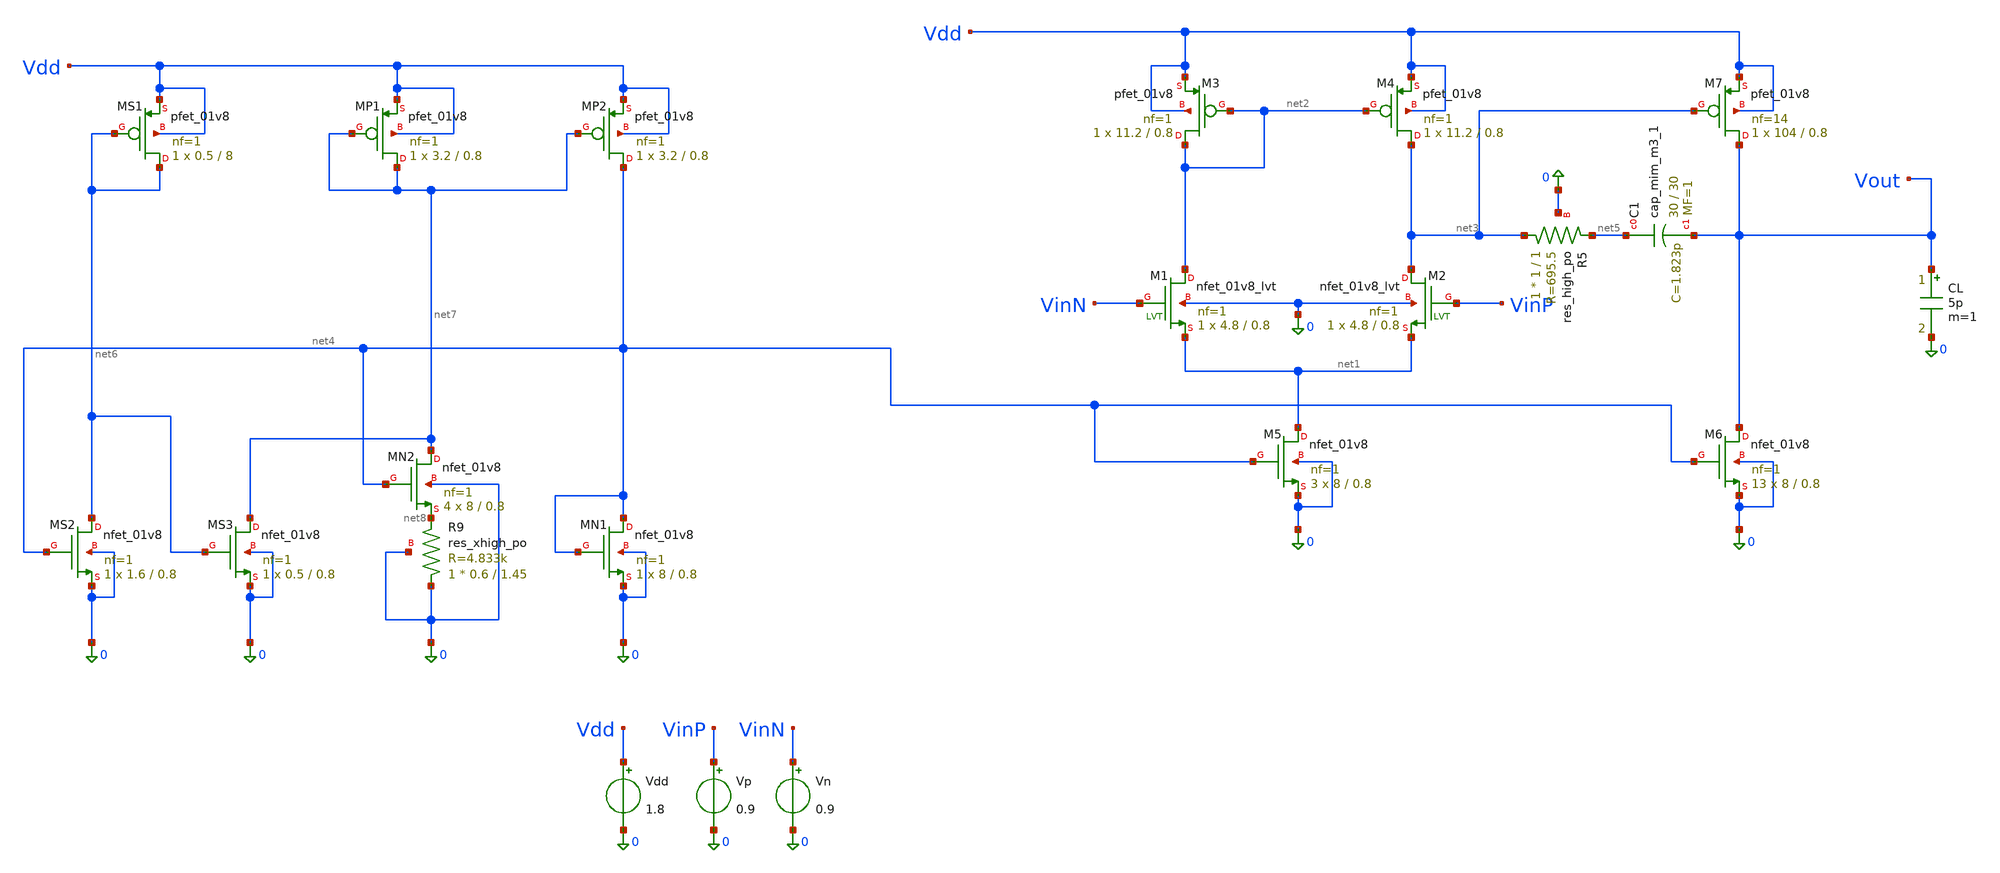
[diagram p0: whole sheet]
** sch_path: parameter_extraction/opamp.sch
**.subckt opamp
XM1 net2 VinN net1 0 sky130_fd_pr__nfet_01v8_lvt L=0.8 W=4.8 nf=1 ad='int((1 + 1)/2) * 4.8 / 1 * 0.29'
+ as='int((1 + 2)/2) * 4.8 / 1 * 0.29' pd='2*int((1 + 1)/2) * (4.8 / 1 + 0.29)' ps='2*int((1 + 2)/2) * (4.8 / 1 + 0.29)'
+ nrd='0.29 / 4.8 ' nrs='0.29 / 4.8 ' sa=0 sb=0 sd=0 mult=1 m=1
XM3 net2 net2 Vdd Vdd sky130_fd_pr__pfet_01v8 L=0.8 W=11.2 nf=1 ad='int((1 + 1)/2) * 11.2 / 1 * 0.29'
+ as='int((1 + 2)/2) * 11.2 / 1 * 0.29' pd='2*int((1 + 1)/2) * (11.2 / 1 + 0.29)' ps='2*int((1 + 2)/2) * (11.2 / 1 + 0.29)'
+ nrd='0.29 / 11.2 ' nrs='0.29 / 11.2 ' sa=0 sb=0 sd=0 mult=1 m=1
XM5 net1 net4 0 0 sky130_fd_pr__nfet_01v8 L=0.8 W=8 nf=1 ad='int((1 + 1)/2) * 8 / 1 * 0.29' as='int((1 + 2)/2) * 8 / 1 * 0.29'
+ pd='2*int((1 + 1)/2) * (8 / 1 + 0.29)' ps='2*int((1 + 2)/2) * (8 / 1 + 0.29)' nrd='0.29 / 8 ' nrs='0.29 / 8 '
+ sa=0 sb=0 sd=0 mult=3 m=3
XM2 net3 VinP net1 0 sky130_fd_pr__nfet_01v8_lvt L=0.8 W=4.8 nf=1 ad='int((1 + 1)/2) * 4.8 / 1 * 0.29'
+ as='int((1 + 2)/2) * 4.8 / 1 * 0.29' pd='2*int((1 + 1)/2) * (4.8 / 1 + 0.29)' ps='2*int((1 + 2)/2) * (4.8 / 1 + 0.29)'
+ nrd='0.29 / 4.8 ' nrs='0.29 / 4.8 ' sa=0 sb=0 sd=0 mult=1 m=1
XM4 net3 net2 Vdd Vdd sky130_fd_pr__pfet_01v8 L=0.8 W=11.2 nf=1 ad='int((1 + 1)/2) * 11.2 / 1 * 0.29'
+ as='int((1 + 2)/2) * 11.2 / 1 * 0.29' pd='2*int((1 + 1)/2) * (11.2 / 1 + 0.29)' ps='2*int((1 + 2)/2) * (11.2 / 1 + 0.29)'
+ nrd='0.29 / 11.2 ' nrs='0.29 / 11.2 ' sa=0 sb=0 sd=0 mult=1 m=1
XM6 Vout net4 0 0 sky130_fd_pr__nfet_01v8 L=0.8 W=8 nf=1 ad='int((1 + 1)/2) * 8 / 1 * 0.29' as='int((1 + 2)/2) * 8 / 1 * 0.29'
+ pd='2*int((1 + 1)/2) * (8 / 1 + 0.29)' ps='2*int((1 + 2)/2) * (8 / 1 + 0.29)' nrd='0.29 / 8 ' nrs='0.29 / 8 '
+ sa=0 sb=0 sd=0 mult=13 m=13
XM7 Vout net3 Vdd Vdd sky130_fd_pr__pfet_01v8 L=0.8 W=104 nf=14 ad='int((14 + 1)/2) * 104 / 14 * 0.29'
+ as='int((14 + 2)/2) * 104 / 14 * 0.29' pd='2*int((14 + 1)/2) * (104 / 14 + 0.29)' ps='2*int((14 + 2)/2) * (104 / 14 + 0.29)'
+ nrd='0.29 / 104 ' nrs='0.29 / 104 ' sa=0 sb=0 sd=0 mult=1 m=1
XC1 net5 Vout sky130_fd_pr__cap_mim_m3_1 W=30 L=30 MF=1 m=1
Vdd Vdd 0 1.8
Vp VinP 0 0.9
Vn VinN 0 0.9
XR5 net3 net5 0 sky130_fd_pr__res_high_po W=1 L=1 mult=1 m=1
CL Vout 0 5p m=1
XMS1 net6 net6 Vdd Vdd sky130_fd_pr__pfet_01v8 L=8 W=0.5 nf=1 ad='int((1 + 1)/2) * 0.5 / 1 * 0.29' as='int((1 + 2)/2) * 0.5 / 1 * 0.29'
+ pd='2*int((1 + 1)/2) * (0.5 / 1 + 0.29)' ps='2*int((1 + 2)/2) * (0.5 / 1 + 0.29)' nrd='0.29 / 0.5 ' nrs='0.29 / 0.5 '
+ sa=0 sb=0 sd=0 mult=1 m=1
XMP1 net7 net7 Vdd Vdd sky130_fd_pr__pfet_01v8 L=0.8 W=3.2 nf=1 ad='int((1 + 1)/2) * 3.2 / 1 * 0.29'
+ as='int((1 + 2)/2) * 3.2 / 1 * 0.29' pd='2*int((1 + 1)/2) * (3.2 / 1 + 0.29)' ps='2*int((1 + 2)/2) * (3.2 / 1 + 0.29)'
+ nrd='0.29 / 3.2 ' nrs='0.29 / 3.2 ' sa=0 sb=0 sd=0 mult=1 m=1
XMP2 net4 net7 Vdd Vdd sky130_fd_pr__pfet_01v8 L=0.8 W=3.2 nf=1 ad='int((1 + 1)/2) * 3.2 / 1 * 0.29'
+ as='int((1 + 2)/2) * 3.2 / 1 * 0.29' pd='2*int((1 + 1)/2) * (3.2 / 1 + 0.29)' ps='2*int((1 + 2)/2) * (3.2 / 1 + 0.29)'
+ nrd='0.29 / 3.2 ' nrs='0.29 / 3.2 ' sa=0 sb=0 sd=0 mult=1 m=1
XR9 0 net8 0 sky130_fd_pr__res_xhigh_po W=0.6 L=1.45 mult=1 m=1
XMS2 net6 net4 0 0 sky130_fd_pr__nfet_01v8 L=0.8 W=1.6 nf=1 ad='int((1 + 1)/2) * 1.6 / 1 * 0.29' as='int((1 + 2)/2) * 1.6 / 1 * 0.29'
+ pd='2*int((1 + 1)/2) * (1.6 / 1 + 0.29)' ps='2*int((1 + 2)/2) * (1.6 / 1 + 0.29)' nrd='0.29 / 1.6 ' nrs='0.29 / 1.6 '
+ sa=0 sb=0 sd=0 mult=1 m=1
XMS3 net7 net6 0 0 sky130_fd_pr__nfet_01v8 L=0.8 W=0.5 nf=1 ad='int((1 + 1)/2) * 0.5 / 1 * 0.29' as='int((1 + 2)/2) * 0.5 / 1 * 0.29'
+ pd='2*int((1 + 1)/2) * (0.5 / 1 + 0.29)' ps='2*int((1 + 2)/2) * (0.5 / 1 + 0.29)' nrd='0.29 / 0.5 ' nrs='0.29 / 0.5 '
+ sa=0 sb=0 sd=0 mult=1 m=1
XMN2 net7 net4 net8 0 sky130_fd_pr__nfet_01v8 L=0.8 W=8 nf=1 ad='int((1 + 1)/2) * 8 / 1 * 0.29' as='int((1 + 2)/2) * 8 / 1 * 0.29'
+ pd='2*int((1 + 1)/2) * (8 / 1 + 0.29)' ps='2*int((1 + 2)/2) * (8 / 1 + 0.29)' nrd='0.29 / 8 ' nrs='0.29 / 8 '
+ sa=0 sb=0 sd=0 mult=4 m=4
XMN1 net4 net4 0 0 sky130_fd_pr__nfet_01v8 L=0.8 W=8 nf=1 ad='int((1 + 1)/2) * 8 / 1 * 0.29' as='int((1 + 2)/2) * 8 / 1 * 0.29'
+ pd='2*int((1 + 1)/2) * (8 / 1 + 0.29)' ps='2*int((1 + 2)/2) * (8 / 1 + 0.29)' nrd='0.29 / 8 ' nrs='0.29 / 8 '
+ sa=0 sb=0 sd=0 mult=1 m=1
**** begin user architecture code


.lib /foss/pdks/sky130A/libs.tech/combined/sky130.lib.spice tt
.option rshunt=1e12

.control
* ======================= user settings =======================
* NOTE: ngspice turns the value of every 'set' variable into lower case,
* so the two file paths are written directly in the lines marked PATH below.
* process corners, temperatures (C) and supply voltages to sweep
set corners = ( tt ss ff sf fs )
set temps   = ( 0 27 85 )
set vdds    = ( 1.8 )
* element names in the testbench
set vddsrc = Vdd
set clname = CL
* internal names of the input transistor M1 and the tail M5 (from 'show m')
set m1 = m.xm1.msky130_fd_pr__nfet_01v8_lvt
set m5 = m.xm5.msky130_fd_pr__nfet_01v8
* load capacitance, compensation capacitance (for the SR estimate), ICMR test points
set clval = 5p
let cc    = 1.5e-12
set vcmlo = 0.8
set vcmhi = 1.1
* ==============================================================

* copy of this netlist up to the code blocks (circuit only, no .lib, no .control)
echo /begin.user.architecture/q > /tmp/opamp_sed.txt
echo w /tmp/opamp_core.cir >> /tmp/opamp_sed.txt
* PATH: the netlist xschem writes for THIS schematic
shell sed -n -f /tmp/opamp_sed.txt /headless/.xschem/simulations/opamp.spice

set labels = ( )
set l_itot = ( )
set l_itail = ( )
set l_sr = ( )
set l_vos = ( )
set l_a0 = ( )
set l_gbw = ( )
set l_pm = ( )
set l_gmarg = ( )
set l_cmrr = ( )
set l_psrr = ( )
set l_noise = ( )
set l_mg1 = ( )
set l_mg5 = ( )

echo
echo  corner temp VDD : Itot(uA) Itail(uA) SR(V/us) Vos(mV) A0(dB) GBW(MHz) PM(deg) GM(dB) CMRR(dB)
+ PSRR(dB) Vn1k(nV/rtHz) M1marg@hi(mV) M5marg@lo(mV)

foreach corner $corners
  echo * corner wrapper > /tmp/opamp_corner_run.cir
* PATH: the SKY130 model library
  echo .lib /foss/pdks/sky130A/libs.tech/combined/sky130.lib.spice $corner >>
+ /tmp/opamp_corner_run.cir
  echo .include /tmp/opamp_core.cir >> /tmp/opamp_corner_run.cir
  echo .option rshunt=1e12 >> /tmp/opamp_corner_run.cir
  echo .end >> /tmp/opamp_corner_run.cir
  source /tmp/opamp_corner_run.cir
  alter $clname c=$clval
  foreach t $temps
    option temp=$t
    foreach vs $vdds
      alter $vddsrc dc=$vs
      alter $vddsrc ac=0
      alter Vp ac=0
      alter Vn ac=0
      alter Vn dc=0.9

* --- operating point and offset (balance the output at 0.9 V)
      dc Vp 0.85 0.95 5u
      meas dc vbal find v(vinp) when v(vout)=0.9
      let vos = (vbal - 0.9)*1e3
      set r_vos = $&vos
      alter Vp dc=$&vbal
      op
      let itot = -i($vddsrc)*1e6
      let itail = @{$m5}[id]*1e6
      let sr = @{$m5}[id]/cc/1e6
      set r_itot = $&itot
      set r_itail = $&itail
      set r_sr = $&sr

* --- open-loop AC
      alter Vp ac=1
      ac dec 30 1 1G
      let ph = 180/pi*cph(v(vout))
      meas ac a0 find vdb(vout) at=1
      meas ac fu when vdb(vout)=0
      meas ac phu find ph at=fu
      meas ac f180 when ph=-180
      meas ac g180 find vdb(vout) at=f180
      let pm = 180 + phu
      let gbw = fu/1e6
      let gmarg = -g180
      set r_a0 = $&a0
      set r_gbw = $&gbw
      set r_pm = $&pm
      set r_gmarg = $&gmarg

* --- CMRR and PSRR at 1 Hz
      alter Vn ac=1
      ac lin 1 1 1
      let acm = vdb(vout)
      let cmrr = $r_a0 - acm
      set r_cmrr = $&cmrr
      alter Vp ac=0
      alter Vn ac=0
      alter $vddsrc ac=1
      ac lin 1 1 1
      let avdd = vdb(vout)
      let psrr = $r_a0 - avdd
      set r_psrr = $&psrr
      alter $vddsrc ac=0
      alter Vp ac=1

* --- input noise at 1 kHz
      noise v(vout) Vp dec 10 100 10k
      setplot previous
      let vn = inoise_spectrum[10]*1e9
      set r_noise = $&vn
      alter Vp ac=0

* --- ICMR edges: M5 margin at the low Vcm, M1 margin at the high Vcm
      alter Vn dc=$vcmlo
      let lo = $vcmlo - 0.05
      let hi = $vcmlo + 0.05
      dc Vp $&lo $&hi 10u
      meas dc vb find v(vinp) when v(vout)=0.9
      alter Vp dc=$&vb
      op
      let mg5 = (@{$m5}[vds] - @{$m5}[vdsat])*1e3
      set r_mg5 = $&mg5
      alter Vn dc=$vcmhi
      let lo = $vcmhi - 0.05
      let hi = $vcmhi + 0.05
      dc Vp $&lo $&hi 10u
      meas dc vb find v(vinp) when v(vout)=0.9
      alter Vp dc=$&vb
      op
      let mg1 = (@{$m1}[vds] - @{$m1}[vdsat])*1e3
      set r_mg1 = $&mg1

* --- print this run and store it
      echo $corner $t $vs : $r_itot $r_itail $r_sr $r_vos $r_a0 $r_gbw $r_pm $r_gmarg $r_cmrr
+ $r_psrr $r_noise $r_mg1 $r_mg5
      set labels  = ( $labels $corner/{$t}C/{$vs}V )
      set l_itot  = ( $l_itot $r_itot )
      set l_itail = ( $l_itail $r_itail )
      set l_sr    = ( $l_sr $r_sr )
      set l_vos   = ( $l_vos $r_vos )
      set l_a0    = ( $l_a0 $r_a0 )
      set l_gbw   = ( $l_gbw $r_gbw )
      set l_pm    = ( $l_pm $r_pm )
      set l_gmarg = ( $l_gmarg $r_gmarg )
      set l_cmrr  = ( $l_cmrr $r_cmrr )
      set l_psrr  = ( $l_psrr $r_psrr )
      set l_noise = ( $l_noise $r_noise )
      set l_mg1   = ( $l_mg1 $r_mg1 )
      set l_mg5   = ( $l_mg5 $r_mg5 )
      alter Vn dc=0.9
    end
  end
  remcirc
end

* ======================= summary: min and max of every spec =======================
setplot new
compose r_itot  values $l_itot
compose r_itail values $l_itail
compose r_sr    values $l_sr
compose r_vos   values $l_vos
compose r_a0    values $l_a0
compose r_gbw   values $l_gbw
compose r_pm    values $l_pm
compose r_gmarg values $l_gmarg
compose r_cmrr  values $l_cmrr
compose r_psrr  values $l_psrr
compose r_noise values $l_noise
compose r_mg1   values $l_mg1
compose r_mg5   values $l_mg5
echo
echo ================ SUMMARY over all corners, temperatures and supplies ================
echo  spec : minimum (where) / maximum (where)
foreach s itot itail sr vos a0 gbw pm gmarg cmrr psrr noise mg1 mg5
  let v = r_{$s}
  let idx = vector(length(v)) + 1
  let vmin = vecmin(v)
  let vmax = vecmax(v)
  let kmin = vecmax(idx*(v le vmin))
  let kmax = vecmax(idx*(v ge vmax))
  set wmin = $labels[$&kmin]
  set wmax = $labels[$&kmax]
  echo $s : $&vmin ( $wmin ) / $&vmax ( $wmax )
end
echo
echo Units: itot, itail uA - sr V/us - vos mV - a0, gmarg, cmrr, psrr dB - gbw MHz - pm deg - noise
+ nV/rtHz at 1 kHz - mg1, mg5 mV (vds-vdsat, must stay positive)
.endc


**** end user architecture code
**.ends
.end
